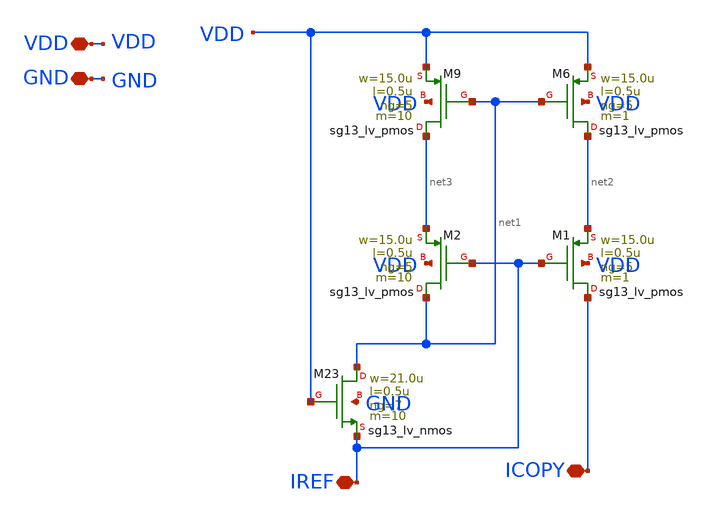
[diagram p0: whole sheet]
** sch_path: blocks/composite/dpi_adexp_neuron/design_data/xschem/sbcmN.sch
**.subckt sbcmN VDD GND IREF ICOPY
*.iopin VDD
*.iopin GND
*.iopin IREF
*.iopin ICOPY
XM6 net2 net1 VDD VDD sg13_lv_pmos w=15.0u l=0.5u ng=5 m=1 mm_ok=1
XM9 net3 net1 VDD VDD sg13_lv_pmos w=15.0u l=0.5u ng=5 m=10 mm_ok=1
XM1 ICOPY IREF net2 VDD sg13_lv_pmos w=15.0u l=0.5u ng=5 m=1 mm_ok=1
XM2 net1 IREF net3 VDD sg13_lv_pmos w=15.0u l=0.5u ng=5 m=10 mm_ok=1
XM23 net1 VDD IREF GND sg13_lv_nmos w=21.0u l=0.5u ng=7 m=10 mm_ok=1
**.ends
.end
